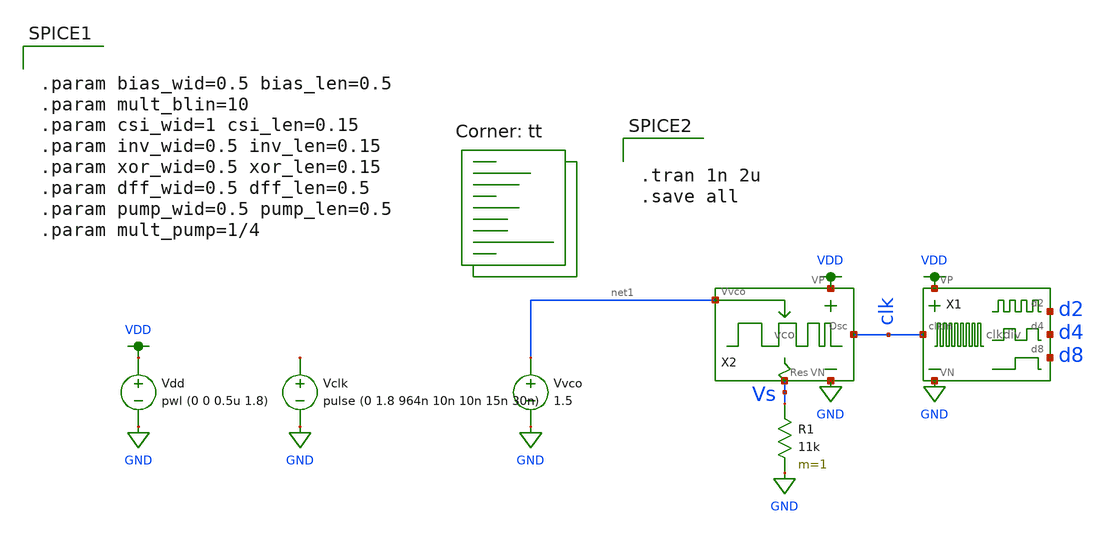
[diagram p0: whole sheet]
** sch_path: test_clkdiv.sch
**.subckt test_clkdiv
Vdd VDD GND pwl (0 0 0.5u 1.8)
Vclk net2 GND pulse (0 1.8 964n 10n 10n 15n 30n)
X1 VDD GND clk d2 d4 d8 clkdiv
R1 Vs GND 11k m=1
X2 VDD GND net1 clk Vs vco
Vvco net1 GND 1.5
**** begin user architecture code


.tran 1n 2u
.save all


.lib $::SKYWATER_MODELS/sky130.lib.spice tt


.param bias_wid=0.5 bias_len=0.5
.param mult_blin=10
.param csi_wid=1 csi_len=0.15
.param inv_wid=0.5 inv_len=0.15
.param xor_wid=0.5 xor_len=0.15
.param dff_wid=0.5 dff_len=0.5
.param pump_wid=0.5 pump_len=0.5
.param mult_pump=1/4


**** end user architecture code
**.ends
.GLOBAL GND
.GLOBAL VDD
.end
